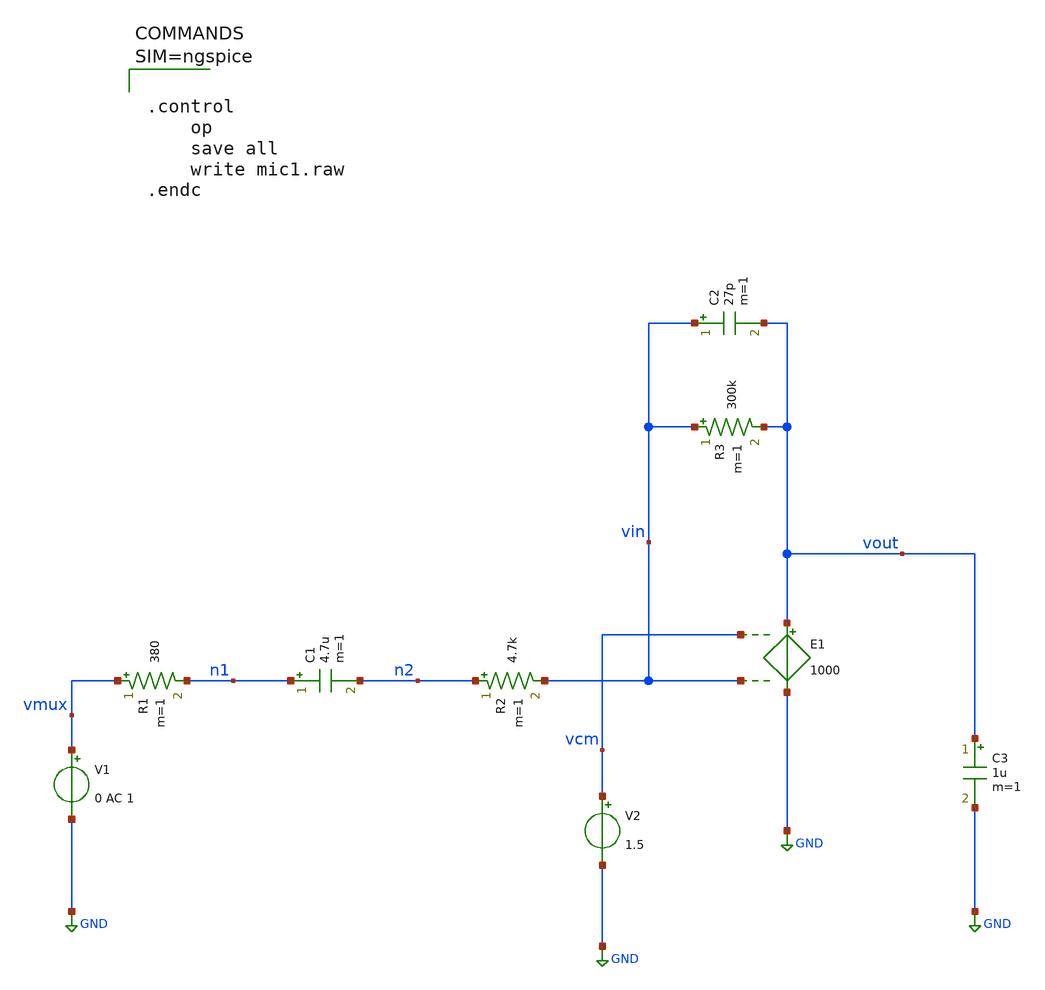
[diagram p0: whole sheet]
** sch_path: xschem/mic1.sch
**.subckt mic1
R1 vmux n1 380 m=1
C1 n1 n2 4.7u m=1
V1 vmux GND 0 AC 1
E1 vout GND vcm vin 1000
R2 n2 vin 4.7k m=1
V2 vcm GND 1.5
R3 vin vout 300k m=1
C2 vin vout 27p m=1
C3 vout GND 1u m=1
**** begin user architecture code



.control
	op
	save all
	write mic1.raw
.endc



**** end user architecture code
**.ends
.GLOBAL GND
.end
